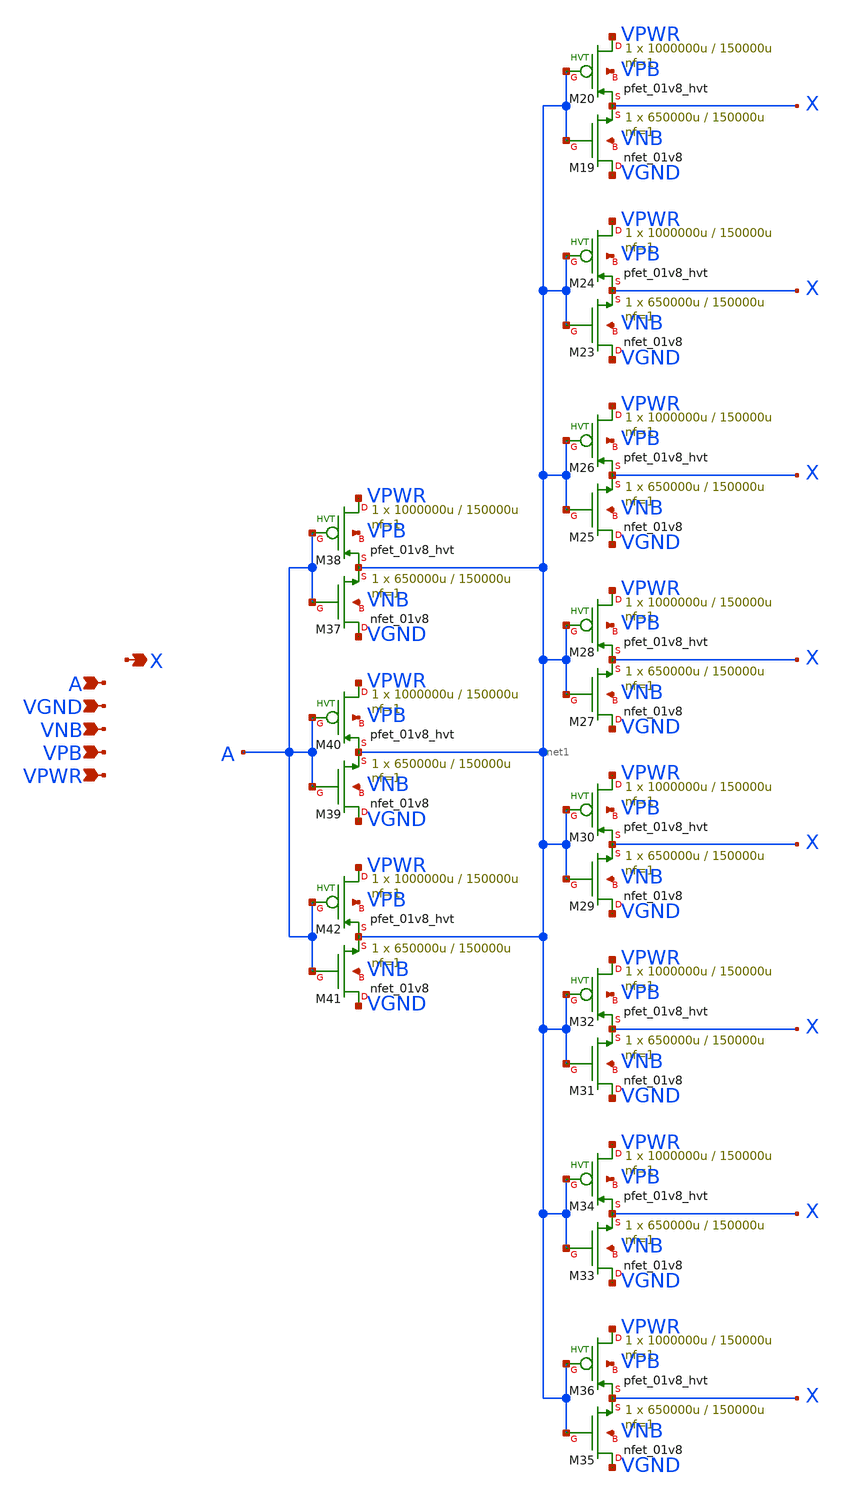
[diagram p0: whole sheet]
** sch_path: schematics/buf/sky130_fd_sc_hd__buf_8.sch
**.subckt sky130_fd_sc_hd__buf_8 A VGND VNB VPB VPWR X
*.ipin A
*.ipin VGND
*.ipin VNB
*.ipin VPB
*.ipin VPWR
*.opin X
XM19 VGND net1 X VNB sky130_fd_pr__nfet_01v8 L=150000u W=650000u nf=1 ad='int((1 + 1)/2) * 650000u / 1 * 0.29'
+ as='int((1 + 2)/2) * 650000u / 1 * 0.29' pd='2*int((1 + 1)/2) * (650000u / 1 + 0.29)' ps='2*int((1 + 2)/2) * (650000u / 1 + 0.29)'
+ nrd='0.29 / 650000u ' nrs='0.29 / 650000u ' sa=0 sb=0 sd=0 mult=1 m=1
XM20 VPWR net1 X VPB sky130_fd_pr__pfet_01v8_hvt L=150000u W=1000000u nf=1 ad='int((1 + 1)/2) * 1000000u / 1 * 0.29'
+ as='int((1 + 2)/2) * 1000000u / 1 * 0.29' pd='2*int((1 + 1)/2) * (1000000u / 1 + 0.29)' ps='2*int((1 + 2)/2) * (1000000u / 1 + 0.29)'
+ nrd='0.29 / 1000000u ' nrs='0.29 / 1000000u ' sa=0 sb=0 sd=0 mult=1 m=1
XM23 VGND net1 X VNB sky130_fd_pr__nfet_01v8 L=150000u W=650000u nf=1 ad='int((1 + 1)/2) * 650000u / 1 * 0.29'
+ as='int((1 + 2)/2) * 650000u / 1 * 0.29' pd='2*int((1 + 1)/2) * (650000u / 1 + 0.29)' ps='2*int((1 + 2)/2) * (650000u / 1 + 0.29)'
+ nrd='0.29 / 650000u ' nrs='0.29 / 650000u ' sa=0 sb=0 sd=0 mult=1 m=1
XM24 VPWR net1 X VPB sky130_fd_pr__pfet_01v8_hvt L=150000u W=1000000u nf=1 ad='int((1 + 1)/2) * 1000000u / 1 * 0.29'
+ as='int((1 + 2)/2) * 1000000u / 1 * 0.29' pd='2*int((1 + 1)/2) * (1000000u / 1 + 0.29)' ps='2*int((1 + 2)/2) * (1000000u / 1 + 0.29)'
+ nrd='0.29 / 1000000u ' nrs='0.29 / 1000000u ' sa=0 sb=0 sd=0 mult=1 m=1
XM25 VGND net1 X VNB sky130_fd_pr__nfet_01v8 L=150000u W=650000u nf=1 ad='int((1 + 1)/2) * 650000u / 1 * 0.29'
+ as='int((1 + 2)/2) * 650000u / 1 * 0.29' pd='2*int((1 + 1)/2) * (650000u / 1 + 0.29)' ps='2*int((1 + 2)/2) * (650000u / 1 + 0.29)'
+ nrd='0.29 / 650000u ' nrs='0.29 / 650000u ' sa=0 sb=0 sd=0 mult=1 m=1
XM26 VPWR net1 X VPB sky130_fd_pr__pfet_01v8_hvt L=150000u W=1000000u nf=1 ad='int((1 + 1)/2) * 1000000u / 1 * 0.29'
+ as='int((1 + 2)/2) * 1000000u / 1 * 0.29' pd='2*int((1 + 1)/2) * (1000000u / 1 + 0.29)' ps='2*int((1 + 2)/2) * (1000000u / 1 + 0.29)'
+ nrd='0.29 / 1000000u ' nrs='0.29 / 1000000u ' sa=0 sb=0 sd=0 mult=1 m=1
XM27 VGND net1 X VNB sky130_fd_pr__nfet_01v8 L=150000u W=650000u nf=1 ad='int((1 + 1)/2) * 650000u / 1 * 0.29'
+ as='int((1 + 2)/2) * 650000u / 1 * 0.29' pd='2*int((1 + 1)/2) * (650000u / 1 + 0.29)' ps='2*int((1 + 2)/2) * (650000u / 1 + 0.29)'
+ nrd='0.29 / 650000u ' nrs='0.29 / 650000u ' sa=0 sb=0 sd=0 mult=1 m=1
XM28 VPWR net1 X VPB sky130_fd_pr__pfet_01v8_hvt L=150000u W=1000000u nf=1 ad='int((1 + 1)/2) * 1000000u / 1 * 0.29'
+ as='int((1 + 2)/2) * 1000000u / 1 * 0.29' pd='2*int((1 + 1)/2) * (1000000u / 1 + 0.29)' ps='2*int((1 + 2)/2) * (1000000u / 1 + 0.29)'
+ nrd='0.29 / 1000000u ' nrs='0.29 / 1000000u ' sa=0 sb=0 sd=0 mult=1 m=1
XM29 VGND net1 X VNB sky130_fd_pr__nfet_01v8 L=150000u W=650000u nf=1 ad='int((1 + 1)/2) * 650000u / 1 * 0.29'
+ as='int((1 + 2)/2) * 650000u / 1 * 0.29' pd='2*int((1 + 1)/2) * (650000u / 1 + 0.29)' ps='2*int((1 + 2)/2) * (650000u / 1 + 0.29)'
+ nrd='0.29 / 650000u ' nrs='0.29 / 650000u ' sa=0 sb=0 sd=0 mult=1 m=1
XM30 VPWR net1 X VPB sky130_fd_pr__pfet_01v8_hvt L=150000u W=1000000u nf=1 ad='int((1 + 1)/2) * 1000000u / 1 * 0.29'
+ as='int((1 + 2)/2) * 1000000u / 1 * 0.29' pd='2*int((1 + 1)/2) * (1000000u / 1 + 0.29)' ps='2*int((1 + 2)/2) * (1000000u / 1 + 0.29)'
+ nrd='0.29 / 1000000u ' nrs='0.29 / 1000000u ' sa=0 sb=0 sd=0 mult=1 m=1
XM31 VGND net1 X VNB sky130_fd_pr__nfet_01v8 L=150000u W=650000u nf=1 ad='int((1 + 1)/2) * 650000u / 1 * 0.29'
+ as='int((1 + 2)/2) * 650000u / 1 * 0.29' pd='2*int((1 + 1)/2) * (650000u / 1 + 0.29)' ps='2*int((1 + 2)/2) * (650000u / 1 + 0.29)'
+ nrd='0.29 / 650000u ' nrs='0.29 / 650000u ' sa=0 sb=0 sd=0 mult=1 m=1
XM32 VPWR net1 X VPB sky130_fd_pr__pfet_01v8_hvt L=150000u W=1000000u nf=1 ad='int((1 + 1)/2) * 1000000u / 1 * 0.29'
+ as='int((1 + 2)/2) * 1000000u / 1 * 0.29' pd='2*int((1 + 1)/2) * (1000000u / 1 + 0.29)' ps='2*int((1 + 2)/2) * (1000000u / 1 + 0.29)'
+ nrd='0.29 / 1000000u ' nrs='0.29 / 1000000u ' sa=0 sb=0 sd=0 mult=1 m=1
XM33 VGND net1 X VNB sky130_fd_pr__nfet_01v8 L=150000u W=650000u nf=1 ad='int((1 + 1)/2) * 650000u / 1 * 0.29'
+ as='int((1 + 2)/2) * 650000u / 1 * 0.29' pd='2*int((1 + 1)/2) * (650000u / 1 + 0.29)' ps='2*int((1 + 2)/2) * (650000u / 1 + 0.29)'
+ nrd='0.29 / 650000u ' nrs='0.29 / 650000u ' sa=0 sb=0 sd=0 mult=1 m=1
XM34 VPWR net1 X VPB sky130_fd_pr__pfet_01v8_hvt L=150000u W=1000000u nf=1 ad='int((1 + 1)/2) * 1000000u / 1 * 0.29'
+ as='int((1 + 2)/2) * 1000000u / 1 * 0.29' pd='2*int((1 + 1)/2) * (1000000u / 1 + 0.29)' ps='2*int((1 + 2)/2) * (1000000u / 1 + 0.29)'
+ nrd='0.29 / 1000000u ' nrs='0.29 / 1000000u ' sa=0 sb=0 sd=0 mult=1 m=1
XM35 VGND net1 X VNB sky130_fd_pr__nfet_01v8 L=150000u W=650000u nf=1 ad='int((1 + 1)/2) * 650000u / 1 * 0.29'
+ as='int((1 + 2)/2) * 650000u / 1 * 0.29' pd='2*int((1 + 1)/2) * (650000u / 1 + 0.29)' ps='2*int((1 + 2)/2) * (650000u / 1 + 0.29)'
+ nrd='0.29 / 650000u ' nrs='0.29 / 650000u ' sa=0 sb=0 sd=0 mult=1 m=1
XM36 VPWR net1 X VPB sky130_fd_pr__pfet_01v8_hvt L=150000u W=1000000u nf=1 ad='int((1 + 1)/2) * 1000000u / 1 * 0.29'
+ as='int((1 + 2)/2) * 1000000u / 1 * 0.29' pd='2*int((1 + 1)/2) * (1000000u / 1 + 0.29)' ps='2*int((1 + 2)/2) * (1000000u / 1 + 0.29)'
+ nrd='0.29 / 1000000u ' nrs='0.29 / 1000000u ' sa=0 sb=0 sd=0 mult=1 m=1
XM37 VGND A net1 VNB sky130_fd_pr__nfet_01v8 L=150000u W=650000u nf=1 ad='int((1 + 1)/2) * 650000u / 1 * 0.29'
+ as='int((1 + 2)/2) * 650000u / 1 * 0.29' pd='2*int((1 + 1)/2) * (650000u / 1 + 0.29)' ps='2*int((1 + 2)/2) * (650000u / 1 + 0.29)'
+ nrd='0.29 / 650000u ' nrs='0.29 / 650000u ' sa=0 sb=0 sd=0 mult=1 m=1
XM38 VPWR A net1 VPB sky130_fd_pr__pfet_01v8_hvt L=150000u W=1000000u nf=1 ad='int((1 + 1)/2) * 1000000u / 1 * 0.29'
+ as='int((1 + 2)/2) * 1000000u / 1 * 0.29' pd='2*int((1 + 1)/2) * (1000000u / 1 + 0.29)' ps='2*int((1 + 2)/2) * (1000000u / 1 + 0.29)'
+ nrd='0.29 / 1000000u ' nrs='0.29 / 1000000u ' sa=0 sb=0 sd=0 mult=1 m=1
XM39 VGND A net1 VNB sky130_fd_pr__nfet_01v8 L=150000u W=650000u nf=1 ad='int((1 + 1)/2) * 650000u / 1 * 0.29'
+ as='int((1 + 2)/2) * 650000u / 1 * 0.29' pd='2*int((1 + 1)/2) * (650000u / 1 + 0.29)' ps='2*int((1 + 2)/2) * (650000u / 1 + 0.29)'
+ nrd='0.29 / 650000u ' nrs='0.29 / 650000u ' sa=0 sb=0 sd=0 mult=1 m=1
XM40 VPWR A net1 VPB sky130_fd_pr__pfet_01v8_hvt L=150000u W=1000000u nf=1 ad='int((1 + 1)/2) * 1000000u / 1 * 0.29'
+ as='int((1 + 2)/2) * 1000000u / 1 * 0.29' pd='2*int((1 + 1)/2) * (1000000u / 1 + 0.29)' ps='2*int((1 + 2)/2) * (1000000u / 1 + 0.29)'
+ nrd='0.29 / 1000000u ' nrs='0.29 / 1000000u ' sa=0 sb=0 sd=0 mult=1 m=1
XM41 VGND A net1 VNB sky130_fd_pr__nfet_01v8 L=150000u W=650000u nf=1 ad='int((1 + 1)/2) * 650000u / 1 * 0.29'
+ as='int((1 + 2)/2) * 650000u / 1 * 0.29' pd='2*int((1 + 1)/2) * (650000u / 1 + 0.29)' ps='2*int((1 + 2)/2) * (650000u / 1 + 0.29)'
+ nrd='0.29 / 650000u ' nrs='0.29 / 650000u ' sa=0 sb=0 sd=0 mult=1 m=1
XM42 VPWR A net1 VPB sky130_fd_pr__pfet_01v8_hvt L=150000u W=1000000u nf=1 ad='int((1 + 1)/2) * 1000000u / 1 * 0.29'
+ as='int((1 + 2)/2) * 1000000u / 1 * 0.29' pd='2*int((1 + 1)/2) * (1000000u / 1 + 0.29)' ps='2*int((1 + 2)/2) * (1000000u / 1 + 0.29)'
+ nrd='0.29 / 1000000u ' nrs='0.29 / 1000000u ' sa=0 sb=0 sd=0 mult=1 m=1
**.ends
.end
